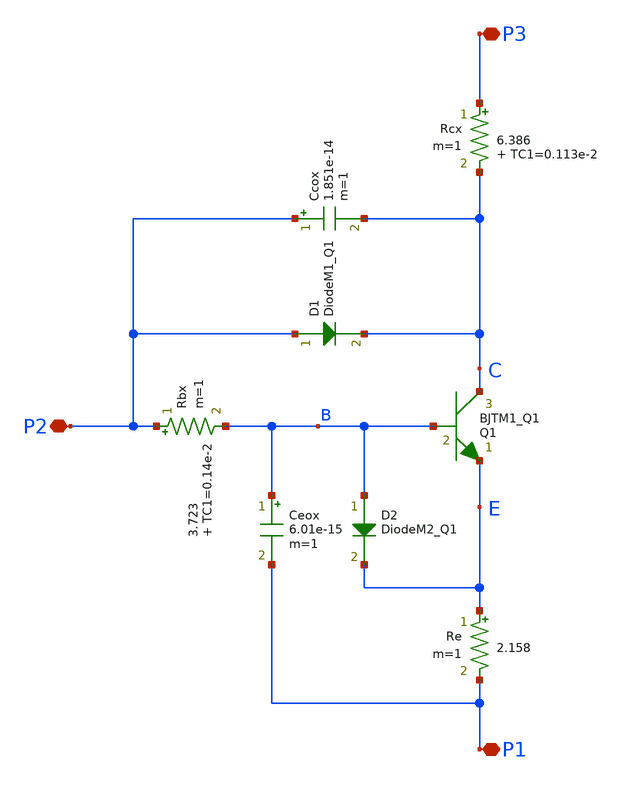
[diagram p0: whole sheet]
** sch_path: xschem_libraries_oa/examples/Q1/schematic/Q1.sch
* Copyright (C) 1998-2024 Stefan Frederik Schippers
* This program is free software; you can redistribute it and/or modify
* it under the terms of the GNU General Public License as published by
* the Free Software Foundation; either version 2 of the License, or
* (at your option) any later version.
* This program is distributed in the hope that it will be useful,
* but WITHOUT ANY WARRANTY; without even the implied warranty of
* MERCHANTABILITY or FITNESS FOR A PARTICULAR PURPOSE.  See the
* GNU General Public License for more details.
* You should have received a copy of the GNU General Public License
* along with this program; if not, write to the Free Software
**.subckt Q1 P3 P1 P2
*.iopin P3
*.iopin P1
*.iopin P2
Rcx P3 C 6.386 TC1=0.113e-2 m=1
Re E P1 2.158 m=1
Rbx P2 B 3.723 TC1=0.14e-2 m=1
Q1 C B E BJTM1_Q1 area=1 m=1
D1 P2 C DiodeM1_Q1 area=1
Ccox P2 C 1.851e-14 m=1
Ceox B P1 6.01e-15 m=1
D2 B E DiodeM2_Q1 area=1
**** begin user architecture code

* This is the BJT model used in the Agilent MSA-26 model
* documented in 5980-2496E.pdf.
* Model entered 3.31.2003 by SDB
.model BJTM1_Q1   NPN(Bf=1e6 IKF=5.895e-1 ISE=2.838e-19 NE=1.006   VAF=44 NF=1 TF=5.37e-12 XTF=20
+ VTF=0.8 ITF=2.218e-1 PTF=22   XTB=0.7 BR=1 IKR=1.1e-2 NC=2 VAR=3.37 NR=1.005 TR=4e-9   EG=1.17 IS=4.475e-18
+ XTI=3 TNOM=21 CJC=2.921e-14   VJC=0.6775 MJC=0.3319 XCJC=4.398e-1 FC=0.8 CJE=7.546e-14    VJE=0.9907
+ MJE=0.5063 RB=9.301 IRB=8.18e-5 RBM=0.1 KF=1.643e-23)

* This is a diode model used in the Agilent MSA-26 model
* documented in 5980-2496E.pdf.
* Model entered 3.31.2003 by SDB
.model DIODEM1_Q1   D(IS=1.405e-17 N=1 CJO=2.281e-14    VJ=0.729 M=0.44 FC=0.8 TNOM=21)

* This is a diode model used in the Agilent MSA-26 model
* documented in 5980-2496E.pdf.
* Model entered 3.31.2003 by SDB
.model DIODEM2_Q1   D(IS=1e-24 N=1.0029 CJO=2.452e-14    VJ=0.8971 M=0.2292 FC=0.8 TNOM=21)




**** end user architecture code
**.ends
.end
